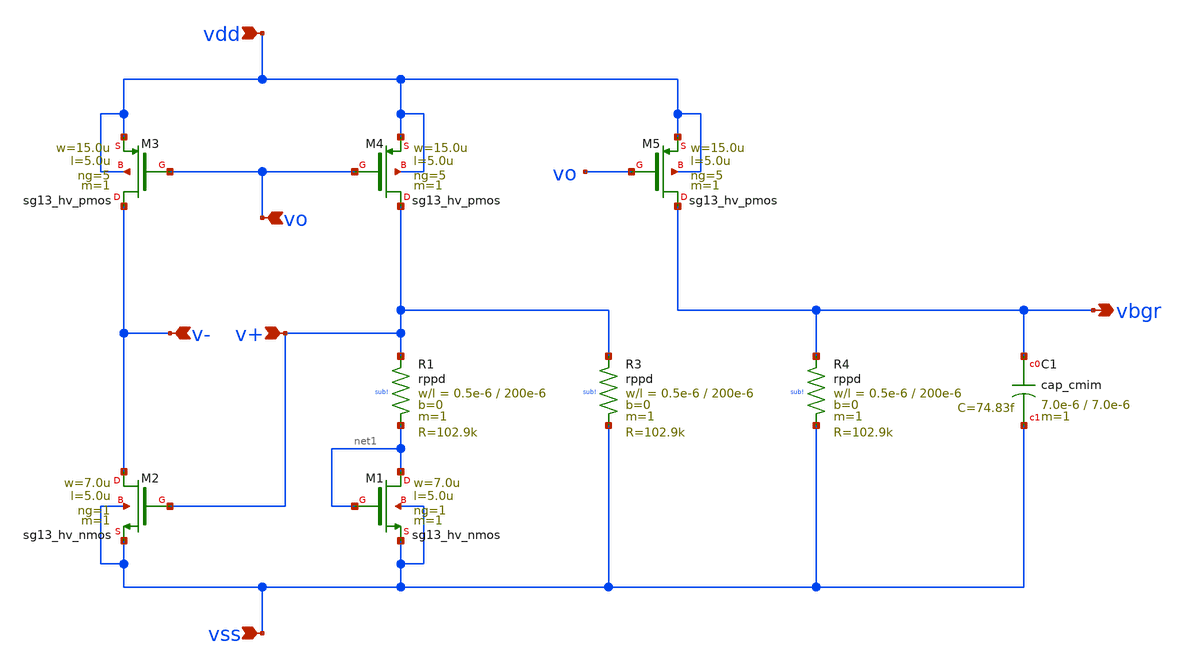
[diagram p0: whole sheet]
** sch_path: schematic/bandgap_ref.sch
**.subckt bandgap_ref vdd vss vo vbgr v+ v-
*.ipin vdd
*.ipin vss
*.ipin vo
*.opin vbgr
*.ipin v+
*.ipin v-
XM1 net1 net1 vss vss sg13_hv_nmos w=7.0u l=5.0u ng=1 m=1 mm_ok=1
XM2 v- v+ vss vss sg13_hv_nmos w=7.0u l=5.0u ng=1 m=1 mm_ok=1
XM3 v- vo vdd vdd sg13_hv_pmos w=15.0u l=5.0u ng=5 m=1 mm_ok=1
XM4 v+ vo vdd vdd sg13_hv_pmos w=15.0u l=5.0u ng=5 m=1 mm_ok=1
XR1 v+ net1 sub! rppd w=0.5e-6 l=200e-6 m=1 b=0 mm_ok=1
XM5 vbgr vo vdd vdd sg13_hv_pmos w=15.0u l=5.0u ng=5 m=1 mm_ok=1
XR3 v+ vss sub! rppd w=0.5e-6 l=200e-6 m=1 b=0 mm_ok=1
XR4 vbgr vss sub! rppd w=0.5e-6 l=200e-6 m=1 b=0 mm_ok=1
XC1 vbgr vss cap_cmim w=7.0e-6 l=7.0e-6 m=1 mm_ok=1
**.ends
.end
